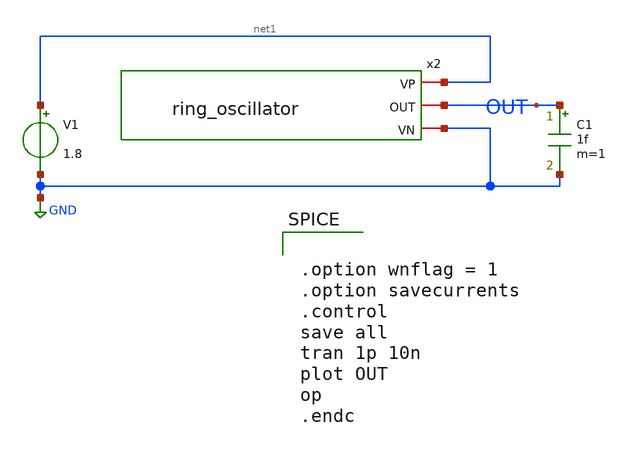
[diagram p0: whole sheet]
** sch_path: ring_oscilator_tb.sch
**.subckt ring_oscilator_tb
C1 OUT GND 1f m=1
V1 net1 GND 1.8
x2 net1 OUT GND ring_oscillator
**** begin user architecture code


.option wnflag = 1
.option savecurrents
.control
save all
tran 1p 10n
plot OUT
op
.endc


 .lib $::SKYWATER_MODELS/sky130.lib.spice tt

.param mc_mm_switch = 0
.param mc_pr_switch = 1

**** end user architecture code
**.ends

* expanding   symbol:  ring_oscillator.sym # of pins=3
** sym_path: ring_oscillator.sym
** sch_path: ring_oscillator.sch
.subckt ring_oscillator VP OUT VN
*.iopin VP
*.iopin VN
*.iopin OUT
x1 VP net1 net2 VN inverter1
x2 VP net2 net3 VN inverter1
x3 VP OUT net1 VN inverter1
x4 VP net3 net4 VN inverter1
x5 VP net4 OUT VN inverter1
.ends


* expanding   symbol:  inverter1.sym # of pins=4
** sym_path: inverter1.sym
** sch_path: inverter1.sch
.subckt inverter1 VP A Y VN
*.ipin A
*.opin Y
*.iopin VP
*.iopin VN
XM1 Y A VN VN sky130_fd_pr__nfet_01v8 L=1 W=0.5 nf=1 ad='int((nf+1)/2) * W/nf * 0.29' as='int((nf+2)/2) * W/nf * 0.29'
+ pd='2*int((nf+1)/2) * (W/nf + 0.29)' ps='2*int((nf+2)/2) * (W/nf + 0.29)' nrd='0.29 / W' nrs='0.29 / W'
+ sa=0 sb=0 sd=0 mult=1 m=1
XM2 Y A VP VP sky130_fd_pr__pfet_01v8 L=0.15 W=1 nf=1 ad='int((nf+1)/2) * W/nf * 0.29' as='int((nf+2)/2) * W/nf * 0.29'
+ pd='2*int((nf+1)/2) * (W/nf + 0.29)' ps='2*int((nf+2)/2) * (W/nf + 0.29)' nrd='0.29 / W' nrs='0.29 / W'
+ sa=0 sb=0 sd=0 mult=1 m=1
.ends

.GLOBAL GND
.end
